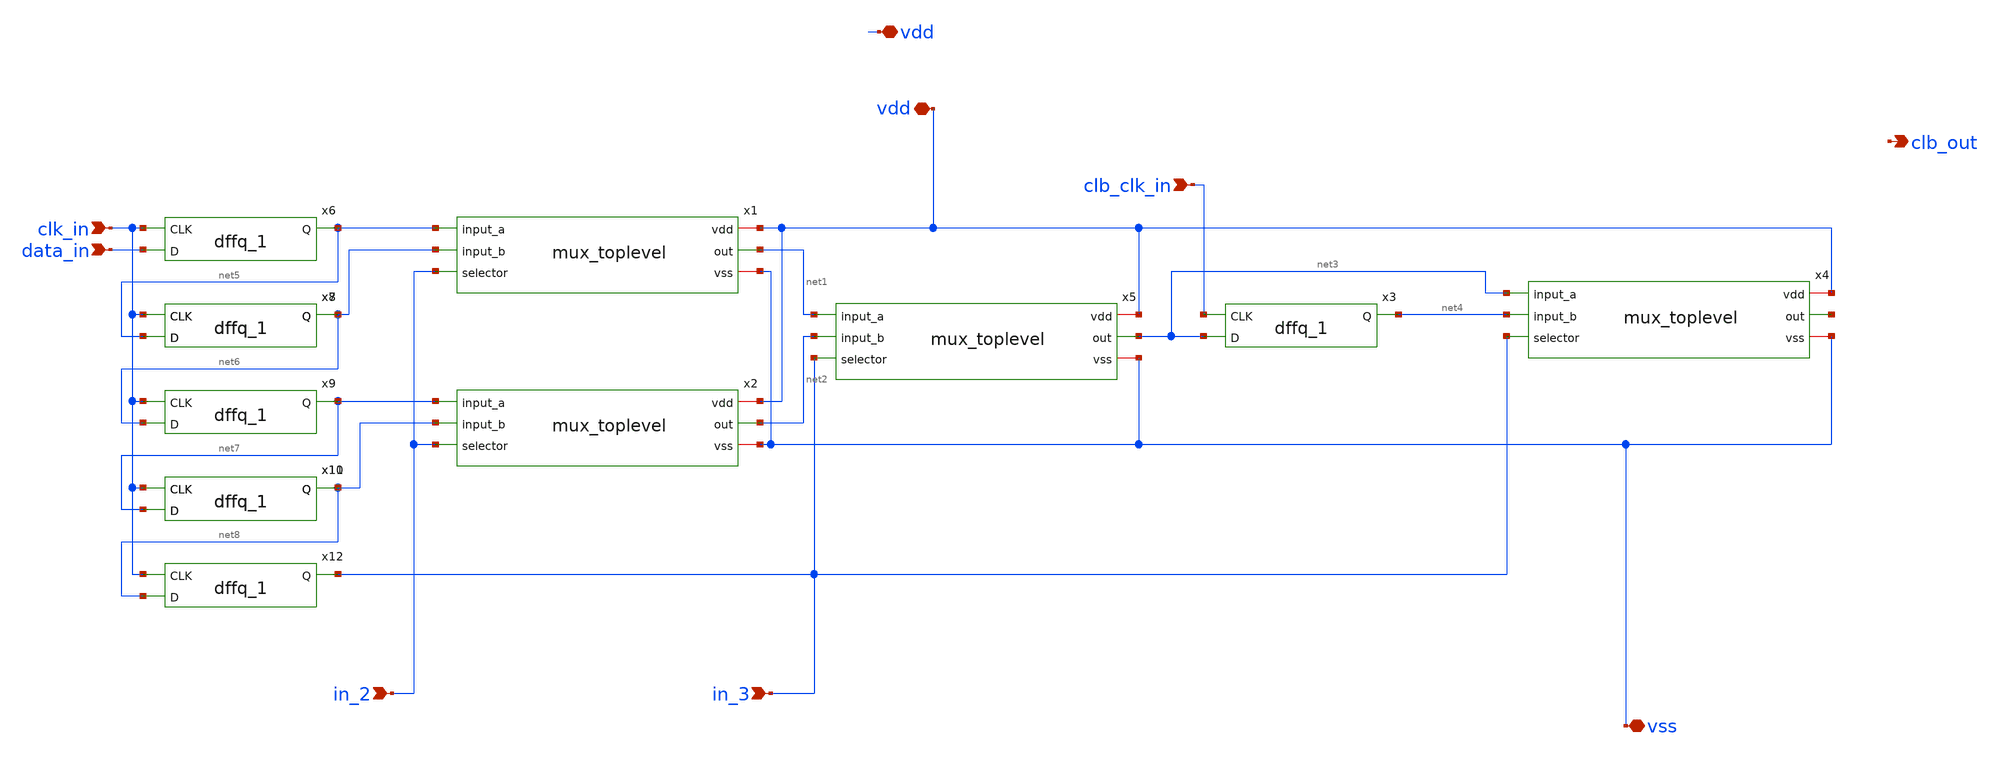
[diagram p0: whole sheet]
** sch_path: designs/libs/core_fpga/clb_3bit/clb_3bit.sch
**.subckt clb_3bit data_in clk_in clb_clk_in vdd vss vdd clb_out in_3 in_2
*.ipin data_in
*.ipin clk_in
*.ipin clb_clk_in
*.iopin vdd
*.iopin vss
*.iopin vdd
*.opin clb_out
*.ipin in_3
*.ipin in_2
x5 vdd net1 net3 net2 in_3 vss mux_toplevel
x3 net3 clb_clk_in net4 VDDd VDDd VSSd VSSd gf180mcu_fd_sc_mcu9t5v0__dffq_1
x1 vdd net5 net1 net6 in_2 vss mux_toplevel
x2 vdd net7 net2 net8 in_2 vss mux_toplevel
x4 vdd net3 net9 net4 in_3 vss mux_toplevel
x6 data_in clk_in net5 VDDd VDDd VSSd VSSd gf180mcu_fd_sc_mcu9t5v0__dffq_1
x7 net5 clk_in net6 VDDd VDDd VSSd VSSd gf180mcu_fd_sc_mcu9t5v0__dffq_1
x8 net5 clk_in net6 VDDd VDDd VSSd VSSd gf180mcu_fd_sc_mcu9t5v0__dffq_1
x9 net6 clk_in net7 VDDd VDDd VSSd VSSd gf180mcu_fd_sc_mcu9t5v0__dffq_1
x10 net7 clk_in net8 VDDd VDDd VSSd VSSd gf180mcu_fd_sc_mcu9t5v0__dffq_1
x11 net7 clk_in net8 VDDd VDDd VSSd VSSd gf180mcu_fd_sc_mcu9t5v0__dffq_1
x12 net8 clk_in in_3 VDDd VDDd VSSd VSSd gf180mcu_fd_sc_mcu9t5v0__dffq_1
**.ends
.end
